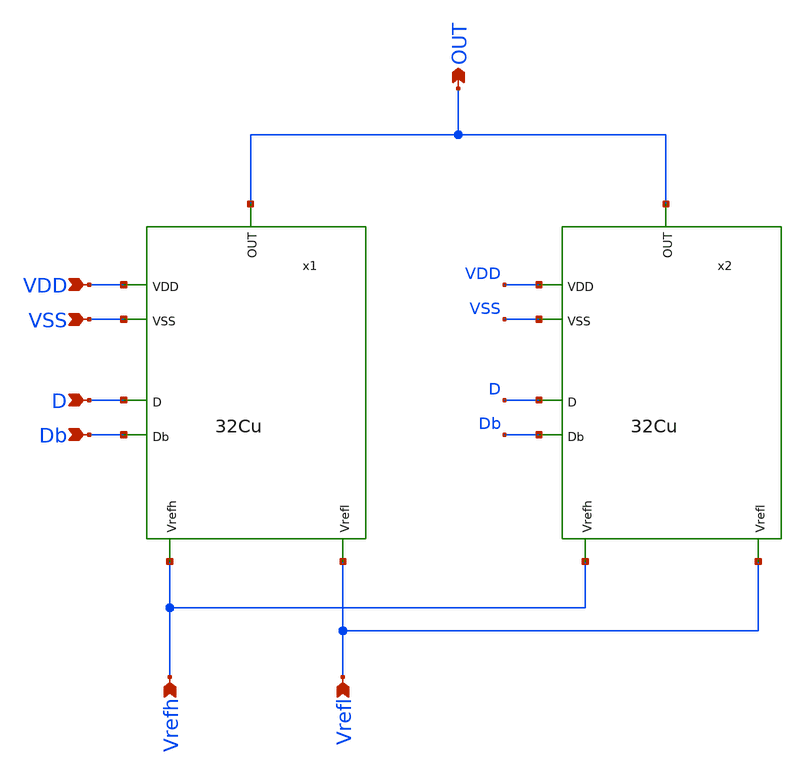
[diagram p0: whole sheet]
** sch_path: 64Cu.sch
**.subckt 64Cu OUT VDD D VSS Vrefh Vrefl Db
*.opin OUT
*.ipin VDD
*.ipin D
*.ipin VSS
*.ipin Vrefh
*.ipin Vrefl
*.ipin Db
x1 OUT VSS VDD Db D Vrefl Vrefh 32Cu
x2 OUT VSS VDD Db D Vrefl Vrefh 32Cu
**.ends
.end
